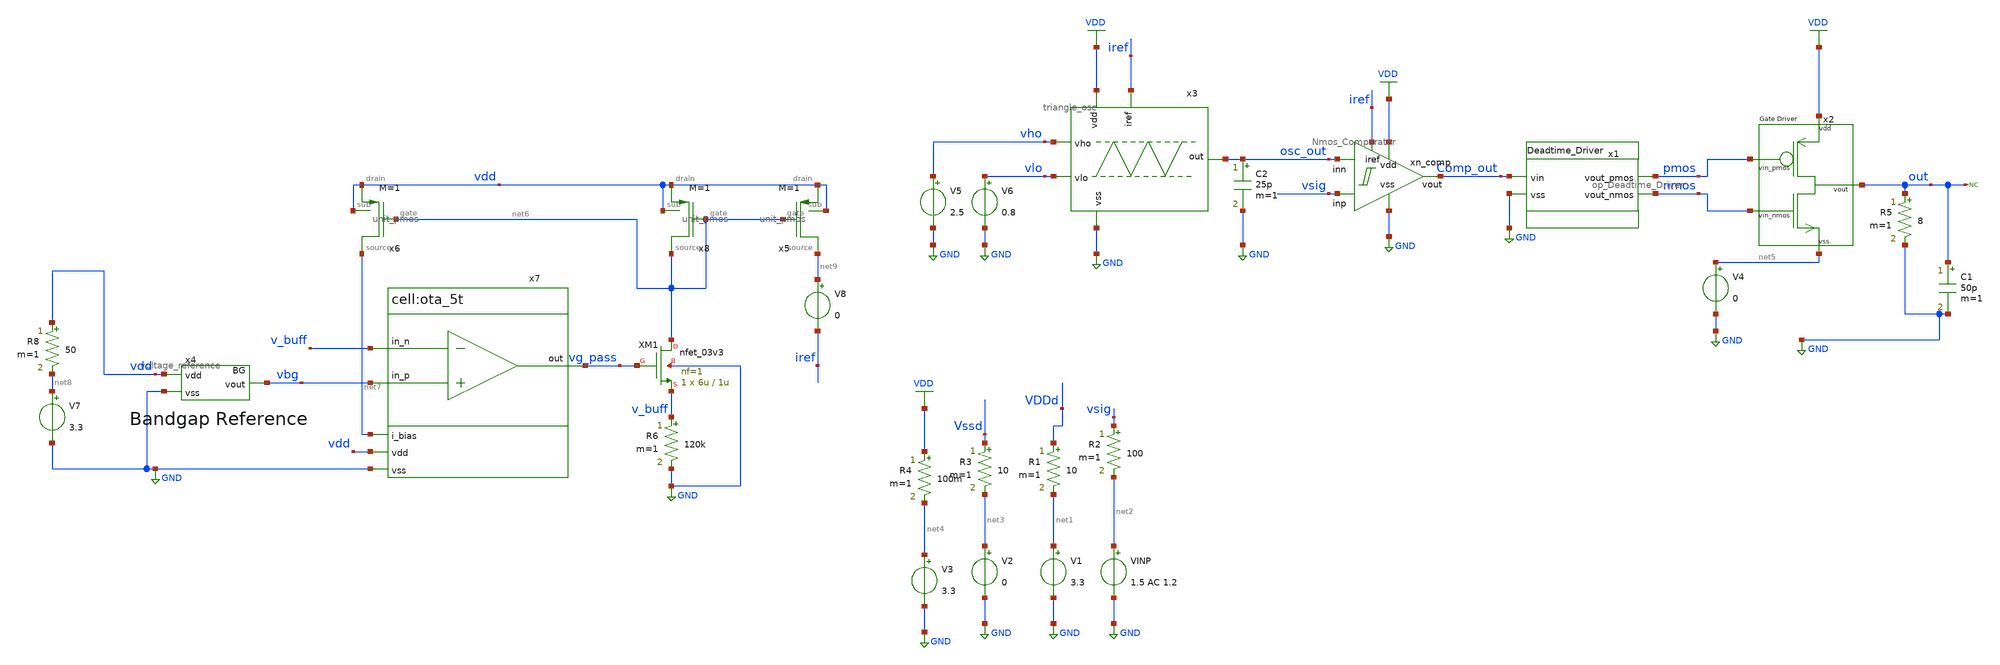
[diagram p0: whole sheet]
** sch_path: designs/libs/tb_analog/tb_top_sim/tb_top_sim.sch
**.subckt tb_top_sim
V1 net1 GND 3.3
VINP net2 GND 1.5 AC 1.2
R1 VDDd net1 10 m=1
R2 vsig net2 100 m=1
V2 net3 GND 0
R3 Vssd net3 10 m=1
x1 pmos Comp_out nmos GND op_Deadtime_Driver
* noconn out
V3 net4 GND 3.3
R4 VDD net4 100m m=1
R5 out GND 8 m=1
C1 out GND 50p m=1
x2 VDD pmos out nmos net5 Output_Stage
V4 net5 GND 0
xn_comp VDD Comp_out vsig GND osc_out iref Nmos_Comparator
x3 VDD vho osc_out vlo iref GND triangle_osc
V5 vho GND 2.5
V6 vlo GND 0.8
C2 osc_out GND 25p m=1
V7 net8 GND 3.3
x4 vdd vbg GND voltage_reference
x5 vdd vdd net6 net9 unit_pmos M=1
R6 v_buff GND 120k m=1
x6 vdd vdd net6 net7 unit_pmos M=1
x7 vdd vg_pass vbg v_buff net7 GND ota_5t
XM1 net6 vg_pass v_buff GND nfet_03v3 L=1u W=6u nf=1 ad='int((nf+1)/2) * W/nf * 0.18u' as='int((nf+2)/2) * W/nf * 0.18u'
+ pd='2*int((nf+1)/2) * (W/nf + 0.18u)' ps='2*int((nf+2)/2) * (W/nf + 0.18u)' nrd='0.18u / W' nrs='0.18u / W'
+ sa=0 sb=0 sd=0 m=1
x8 vdd vdd net6 net6 unit_pmos M=1
R8 vdd net8 50 m=1
V8 net9 iref 0
**** begin user architecture code

.include $::180MCU_MODELS/design.ngspice
.include /foss/pdks/gf180mcuD/libs.ref/gf180mcu_fd_sc_mcu9t5v0/spice/gf180mcu_fd_sc_mcu9t5v0.spice
.lib $::180MCU_MODELS/sm141064.ngspice typical
.lib $::180MCU_MODELS/sm141064.ngspice cap_mim
.lib $::180MCU_MODELS/sm141064.ngspice mimcap_typical
.lib $::180MCU_MODELS/sm141064.ngspice res_typical
.lib $::180MCU_MODELS/sm141064.ngspice moscap_typical
.lib $::180MCU_MODELS/sm141064.ngspice bjt_typical



.temp 27
.param Tbit = 20n
.ic v(osc_out)=0
.options savecurrents
.global VDDd VSSd
.control
save all
**Frequency & time settings
let fsig = 20k
let tper=1/fsig
let tfr = 0.5*tper
let ton = 0.5*tper-2*tfr

let tstop = 4 * tper
let tstep = 0.001*tper


**voltages
*alter @VINP[PULSE] = [ 0 3.0 1u $&tfr $&tfr $&ton $&tper 3 ]
alter @VINP[DC] = 2
alter @VINP[SIN] = [ 1.6 0.4 $&fsig 0 0 ]

**simulation
OP
*show all > op.log
show all

**Temperature analysis
tran 5n 200u 0
let t = $temp
print t

**voltage reference analysis
plot v8#branch

**oscillator & comparator analysis
*plot osc_out vsig Comp_out
plot Comp_out

**deadtime & driver analysis
*plot nmos pmos
*plot out

meas tran tfall_p WHEN v(pmos)=0.68 FALL=2
meas tran tfall_n WHEN v(nmos)=0.68 FALL=2

meas tran trise_p WHEN v(pmos)=0.68 RISE=2
meas tran trise_n WHEN v(nmos)=0.68 RISE=2

let delay_fall = $&tfall_p - $&tfall_n
let delay_rise = $&trise_p - $&trise_n

print delay_fall
print delay_rise

meas tran v_max MAX v(out)
meas tran v_min MIN v(out)
let vpp = $&v_max - $&v_min
print vpp

**check shoot-through analysis
plot @r5[i] v3#branch v4#branch
*@m.xm1.m0[id]
*plot @m.xm1.m0[id]
plot v4#branch


write Full_Output_Stage_tb.txt
.endc


**** end user architecture code
**.ends
.GLOBAL GND
.GLOBAL VDD
.end
